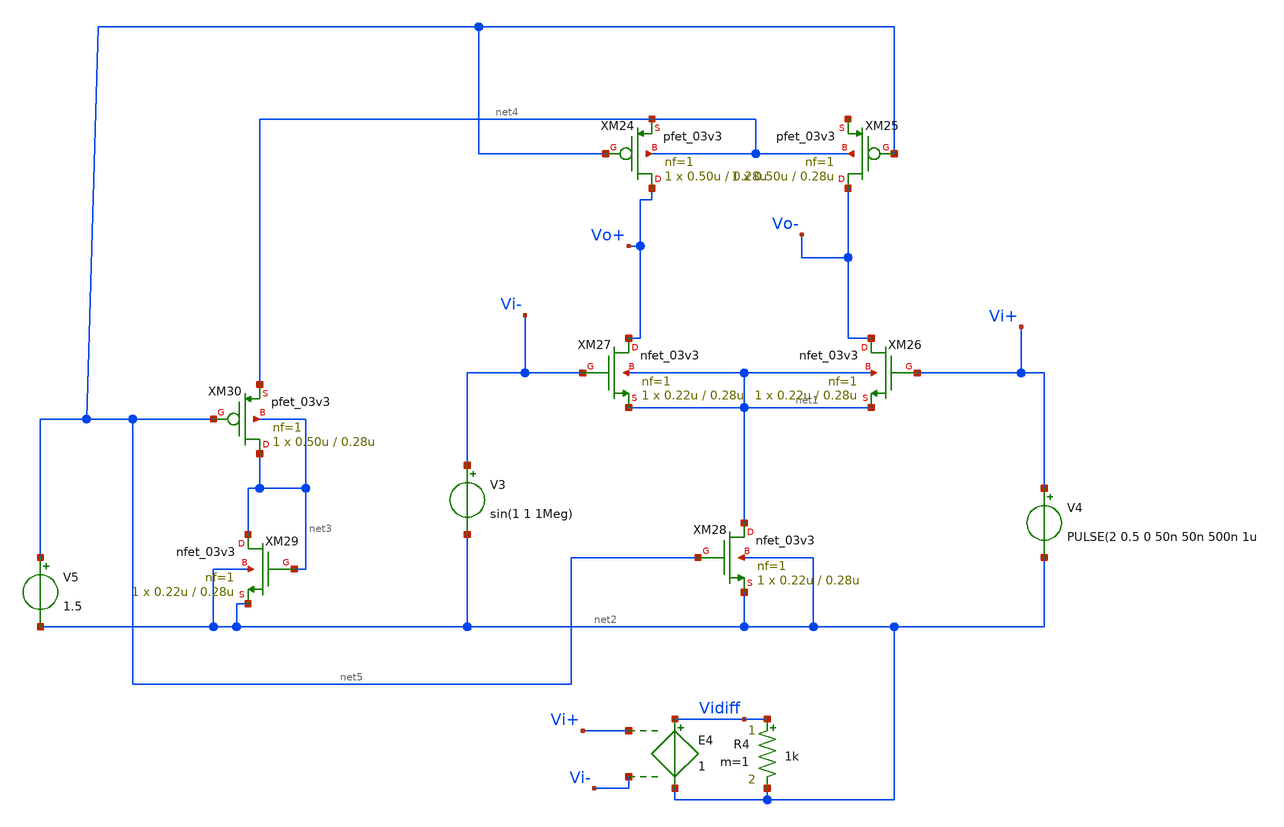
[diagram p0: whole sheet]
** sch_path: old/untitled.sch
**.subckt untitled
XM26 Vo- Vi+ net1 net1 nfet_03v3 L=0.28u W=0.22u nf=1 ad='int((nf+1)/2) * W/nf * 0.18u' as='int((nf+2)/2) * W/nf * 0.18u'
+ pd='2*int((nf+1)/2) * (W/nf + 0.18u)' ps='2*int((nf+2)/2) * (W/nf + 0.18u)' nrd='0.18u / W' nrs='0.18u / W'
+ sa=0 sb=0 sd=0 m=1
XM27 Vo+ Vi- net1 net1 nfet_03v3 L=0.28u W=0.22u nf=1 ad='int((nf+1)/2) * W/nf * 0.18u' as='int((nf+2)/2) * W/nf * 0.18u'
+ pd='2*int((nf+1)/2) * (W/nf + 0.18u)' ps='2*int((nf+2)/2) * (W/nf + 0.18u)' nrd='0.18u / W' nrs='0.18u / W'
+ sa=0 sb=0 sd=0 m=1
V3 Vi- net2 sin(1 1 1Meg)
V4 Vi+ net2 PULSE(2 0.5 0 50n 50n 500n 1u
R4 Vidiff net2 1k m=1
E4 Vidiff net2 Vi+ Vi- 1
XM28 net1 net5 net2 net2 nfet_03v3 L=0.28u W=0.22u nf=1 ad='int((nf+1)/2) * W/nf * 0.18u' as='int((nf+2)/2) * W/nf * 0.18u'
+ pd='2*int((nf+1)/2) * (W/nf + 0.18u)' ps='2*int((nf+2)/2) * (W/nf + 0.18u)' nrd='0.18u / W' nrs='0.18u / W'
+ sa=0 sb=0 sd=0 m=1
XM29 net3 net3 net2 net2 nfet_03v3 L=0.28u W=0.22u nf=1 ad='int((nf+1)/2) * W/nf * 0.18u' as='int((nf+2)/2) * W/nf * 0.18u'
+ pd='2*int((nf+1)/2) * (W/nf + 0.18u)' ps='2*int((nf+2)/2) * (W/nf + 0.18u)' nrd='0.18u / W' nrs='0.18u / W'
+ sa=0 sb=0 sd=0 m=1
V5 net5 net2 1.5
XM30 net3 net5 net4 net3 pfet_03v3 L=0.28u W=0.50u nf=1 ad='int((nf+1)/2) * W/nf * 0.18u' as='int((nf+2)/2) * W/nf * 0.18u'
+ pd='2*int((nf+1)/2) * (W/nf + 0.18u)' ps='2*int((nf+2)/2) * (W/nf + 0.18u)' nrd='0.18u / W' nrs='0.18u / W'
+ sa=0 sb=0 sd=0 m=1
XM24 Vo+ net5 net4 net4 pfet_03v3 L=0.28u W=0.50u nf=1 ad='int((nf+1)/2) * W/nf * 0.18u' as='int((nf+2)/2) * W/nf * 0.18u'
+ pd='2*int((nf+1)/2) * (W/nf + 0.18u)' ps='2*int((nf+2)/2) * (W/nf + 0.18u)' nrd='0.18u / W' nrs='0.18u / W'
+ sa=0 sb=0 sd=0 m=1
XM25 Vo- net5 net6 net4 pfet_03v3 L=0.28u W=0.50u nf=1 ad='int((nf+1)/2) * W/nf * 0.18u' as='int((nf+2)/2) * W/nf * 0.18u'
+ pd='2*int((nf+1)/2) * (W/nf + 0.18u)' ps='2*int((nf+2)/2) * (W/nf + 0.18u)' nrd='0.18u / W' nrs='0.18u / W'
+ sa=0 sb=0 sd=0 m=1
**.ends
.end
